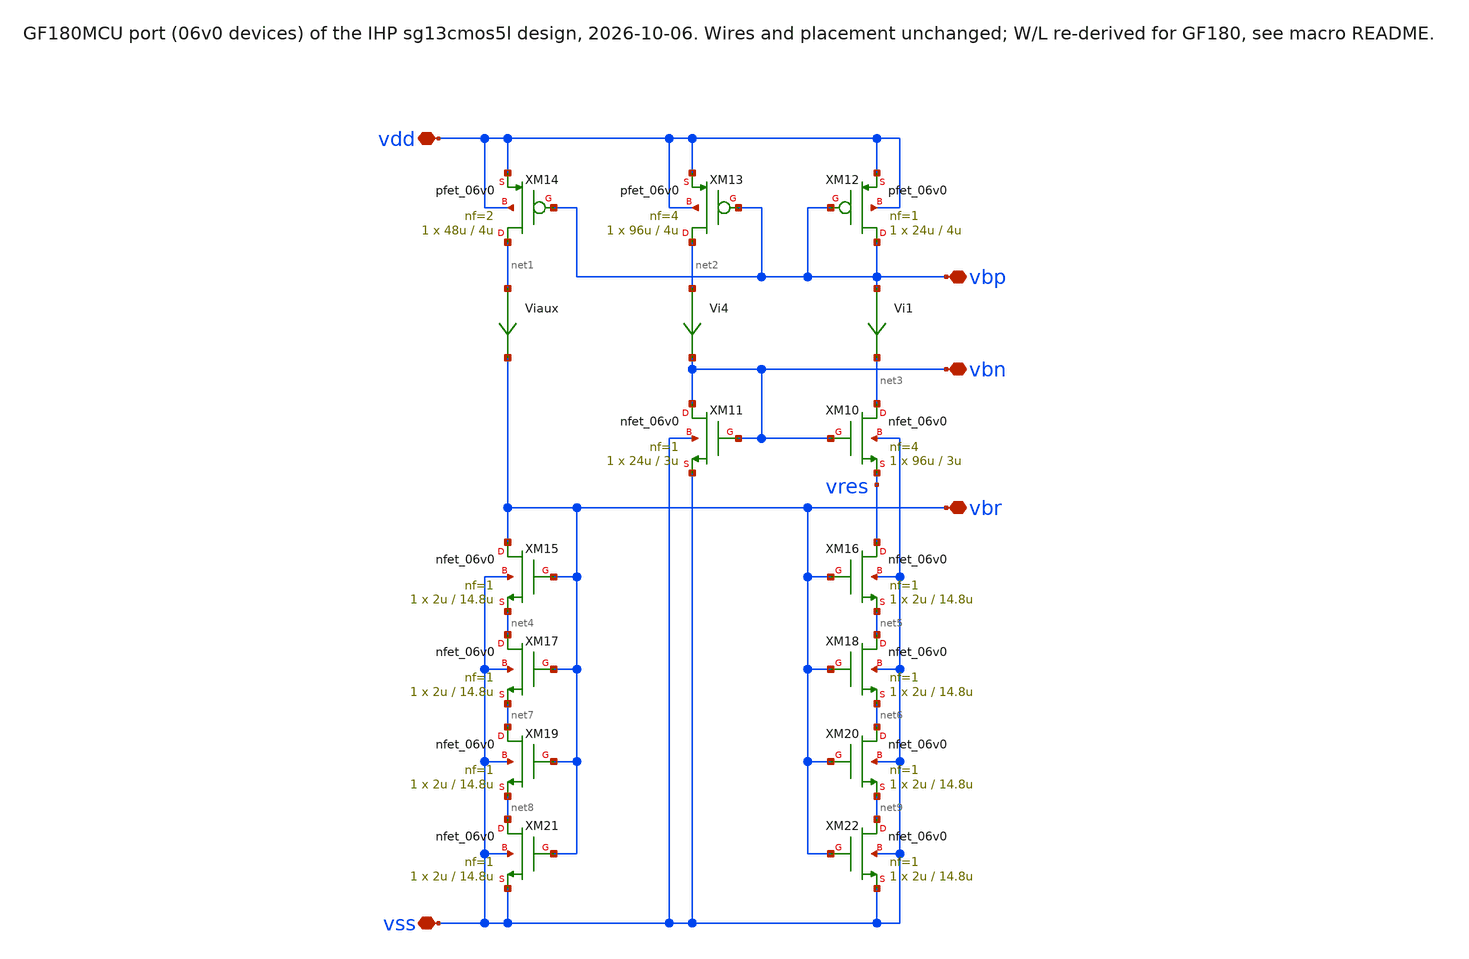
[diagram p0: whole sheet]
** sch_path: macros/OgueyAebischerBias/schematic/xschem/OgueyAebischerBias_06v0.sch
**.subckt OgueyAebischerBias_06v0 vss vdd vbp vbn vbr
*.iopin vss
*.iopin vdd
*.iopin vbp
*.iopin vbn
*.iopin vbr
XM10 net3 vbn vres vss nfet_06v0 L=3u W=96u nf=4 ad='int((nf+1)/2) * W/nf * 0.18u' as='int((nf+2)/2) * W/nf * 0.18u'
+ pd='2*int((nf+1)/2) * (W/nf + 0.18u)' ps='2*int((nf+2)/2) * (W/nf + 0.18u)' nrd='0.18u / W' nrs='0.18u / W'
+ sa=0 sb=0 sd=0 m=1
XM12 vbp vbp vdd vdd pfet_06v0 L=4u W=24u nf=1 ad='int((nf+1)/2) * W/nf * 0.18u' as='int((nf+2)/2) * W/nf * 0.18u'
+ pd='2*int((nf+1)/2) * (W/nf + 0.18u)' ps='2*int((nf+2)/2) * (W/nf + 0.18u)' nrd='0.18u / W' nrs='0.18u / W'
+ sa=0 sb=0 sd=0 m=1
XM11 vbn vbn vss vss nfet_06v0 L=3u W=24u nf=1 ad='int((nf+1)/2) * W/nf * 0.18u' as='int((nf+2)/2) * W/nf * 0.18u'
+ pd='2*int((nf+1)/2) * (W/nf + 0.18u)' ps='2*int((nf+2)/2) * (W/nf + 0.18u)' nrd='0.18u / W' nrs='0.18u / W'
+ sa=0 sb=0 sd=0 m=1
XM13 net2 vbp vdd vdd pfet_06v0 L=4u W=96u nf=4 ad='int((nf+1)/2) * W/nf * 0.18u' as='int((nf+2)/2) * W/nf * 0.18u'
+ pd='2*int((nf+1)/2) * (W/nf + 0.18u)' ps='2*int((nf+2)/2) * (W/nf + 0.18u)' nrd='0.18u / W' nrs='0.18u / W'
+ sa=0 sb=0 sd=0 m=1
XM14 net1 vbp vdd vdd pfet_06v0 L=4u W=48u nf=2 ad='int((nf+1)/2) * W/nf * 0.18u' as='int((nf+2)/2) * W/nf * 0.18u'
+ pd='2*int((nf+1)/2) * (W/nf + 0.18u)' ps='2*int((nf+2)/2) * (W/nf + 0.18u)' nrd='0.18u / W' nrs='0.18u / W'
+ sa=0 sb=0 sd=0 m=1
XM16 vres vbr net5 vss nfet_06v0 L=14.8u W=2u nf=1 ad='int((nf+1)/2) * W/nf * 0.18u' as='int((nf+2)/2) * W/nf * 0.18u'
+ pd='2*int((nf+1)/2) * (W/nf + 0.18u)' ps='2*int((nf+2)/2) * (W/nf + 0.18u)' nrd='0.18u / W' nrs='0.18u / W'
+ sa=0 sb=0 sd=0 m=1
XM15 vbr vbr net4 vss nfet_06v0 L=14.8u W=2u nf=1 ad='int((nf+1)/2) * W/nf * 0.18u' as='int((nf+2)/2) * W/nf * 0.18u'
+ pd='2*int((nf+1)/2) * (W/nf + 0.18u)' ps='2*int((nf+2)/2) * (W/nf + 0.18u)' nrd='0.18u / W' nrs='0.18u / W'
+ sa=0 sb=0 sd=0 m=1
Vi1 vbp net3 0
.save i(vi1)
Vi4 net2 vbn 0
.save i(vi4)
Viaux net1 vbr 0
.save i(viaux)
XM18 net5 vbr net6 vss nfet_06v0 L=14.8u W=2u nf=1 ad='int((nf+1)/2) * W/nf * 0.18u' as='int((nf+2)/2) * W/nf * 0.18u'
+ pd='2*int((nf+1)/2) * (W/nf + 0.18u)' ps='2*int((nf+2)/2) * (W/nf + 0.18u)' nrd='0.18u / W' nrs='0.18u / W'
+ sa=0 sb=0 sd=0 m=1
XM17 net4 vbr net7 vss nfet_06v0 L=14.8u W=2u nf=1 ad='int((nf+1)/2) * W/nf * 0.18u' as='int((nf+2)/2) * W/nf * 0.18u'
+ pd='2*int((nf+1)/2) * (W/nf + 0.18u)' ps='2*int((nf+2)/2) * (W/nf + 0.18u)' nrd='0.18u / W' nrs='0.18u / W'
+ sa=0 sb=0 sd=0 m=1
XM20 net6 vbr net9 vss nfet_06v0 L=14.8u W=2u nf=1 ad='int((nf+1)/2) * W/nf * 0.18u' as='int((nf+2)/2) * W/nf * 0.18u'
+ pd='2*int((nf+1)/2) * (W/nf + 0.18u)' ps='2*int((nf+2)/2) * (W/nf + 0.18u)' nrd='0.18u / W' nrs='0.18u / W'
+ sa=0 sb=0 sd=0 m=1
XM19 net7 vbr net8 vss nfet_06v0 L=14.8u W=2u nf=1 ad='int((nf+1)/2) * W/nf * 0.18u' as='int((nf+2)/2) * W/nf * 0.18u'
+ pd='2*int((nf+1)/2) * (W/nf + 0.18u)' ps='2*int((nf+2)/2) * (W/nf + 0.18u)' nrd='0.18u / W' nrs='0.18u / W'
+ sa=0 sb=0 sd=0 m=1
XM22 net9 vbr vss vss nfet_06v0 L=14.8u W=2u nf=1 ad='int((nf+1)/2) * W/nf * 0.18u' as='int((nf+2)/2) * W/nf * 0.18u'
+ pd='2*int((nf+1)/2) * (W/nf + 0.18u)' ps='2*int((nf+2)/2) * (W/nf + 0.18u)' nrd='0.18u / W' nrs='0.18u / W'
+ sa=0 sb=0 sd=0 m=1
XM21 net8 vbr vss vss nfet_06v0 L=14.8u W=2u nf=1 ad='int((nf+1)/2) * W/nf * 0.18u' as='int((nf+2)/2) * W/nf * 0.18u'
+ pd='2*int((nf+1)/2) * (W/nf + 0.18u)' ps='2*int((nf+2)/2) * (W/nf + 0.18u)' nrd='0.18u / W' nrs='0.18u / W'
+ sa=0 sb=0 sd=0 m=1
**.ends
.end
